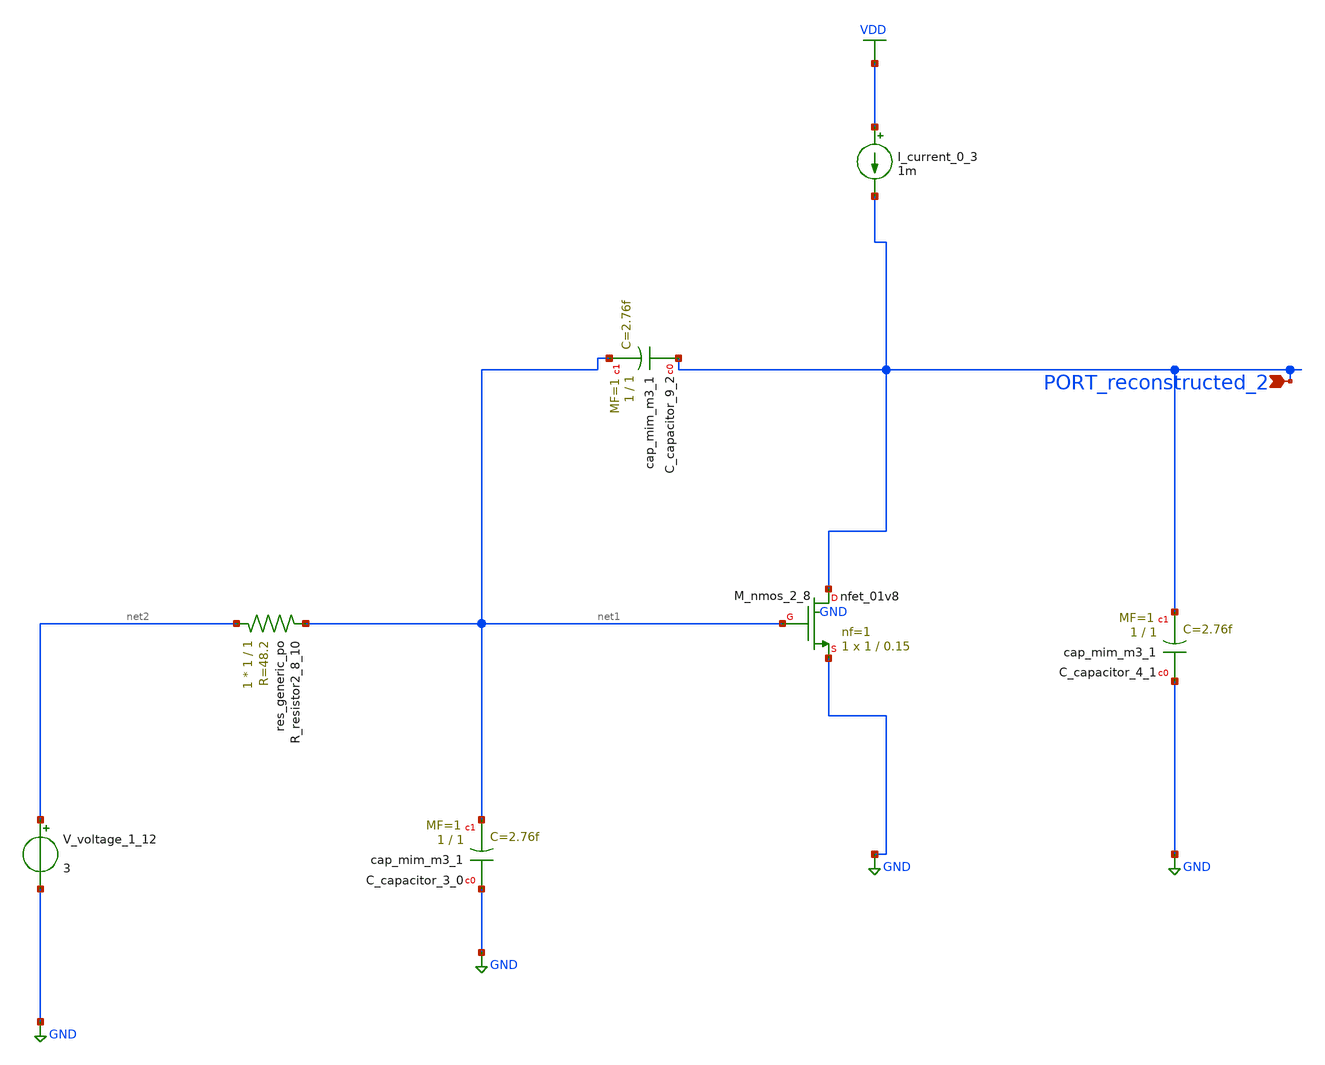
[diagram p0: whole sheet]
** sch_path: schematics/AMSNet/364.sch
**.subckt 364 PORT_reconstructed_2
*.ipin PORT_reconstructed_2
XC_capacitor_3_0 GND net1 sky130_fd_pr__cap_mim_m3_1 W=1 L=1 MF=1 m=1
XC_capacitor_4_1 GND PORT_reconstructed_2 sky130_fd_pr__cap_mim_m3_1 W=1 L=1 MF=1 m=1
XC_capacitor_9_2 PORT_reconstructed_2 net1 sky130_fd_pr__cap_mim_m3_1 W=1 L=1 MF=1 m=1
I_current_0_3 VDD PORT_reconstructed_2 1m
XM_nmos_2_8 PORT_reconstructed_2 net1 GND GND sky130_fd_pr__nfet_01v8 L=0.15 W=1 nf=1 ad='int((1 + 1)/2) * 1 / 1 * 0.29'
+ as='int((1 + 2)/2) * 1 / 1 * 0.29' pd='2*int((1 + 1)/2) * (1 / 1 + 0.29)' ps='2*int((1 + 2)/2) * (1 / 1 + 0.29)'
+ nrd='0.29 / 1 ' nrs='0.29 / 1 ' sa=0 sb=0 sd=0 mult=1 m=1
XR_resistor2_8_10 net2 net1 sky130_fd_pr__res_generic_po W=1 L=1 m=1
V_voltage_1_12 net2 GND 3
**.ends
.GLOBAL GND
.GLOBAL VDD
.end
